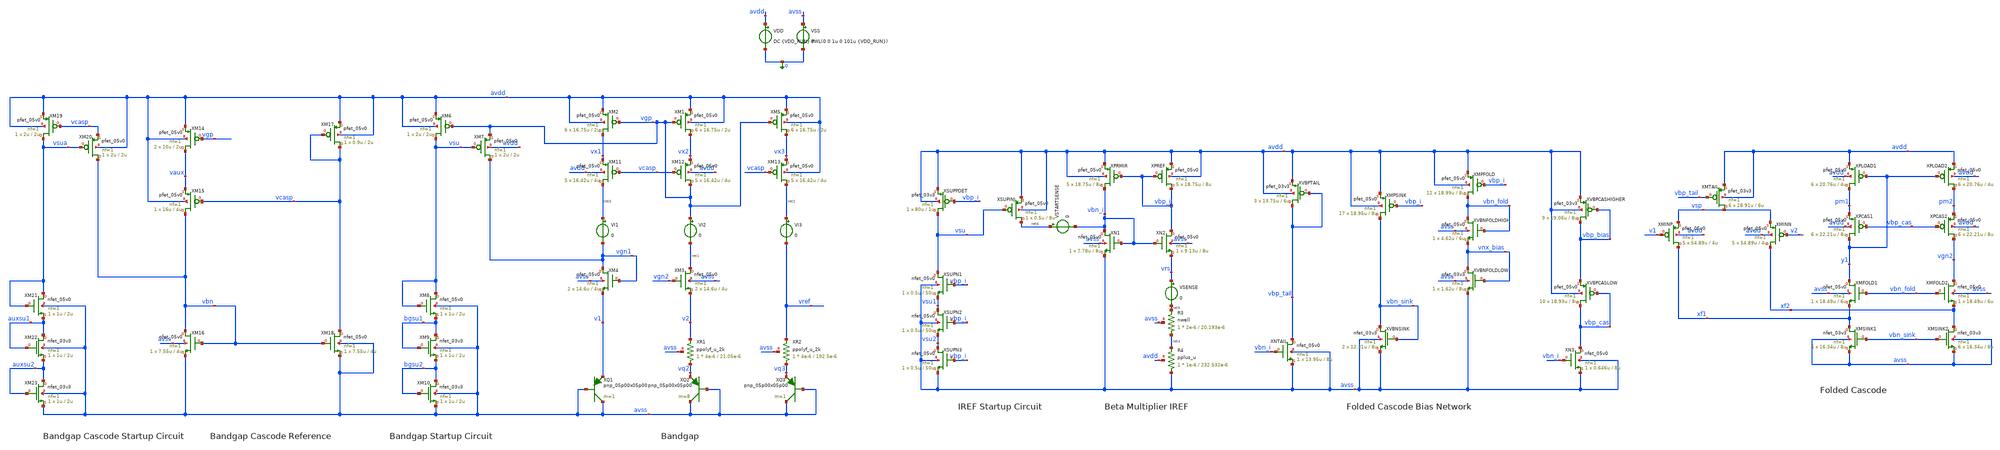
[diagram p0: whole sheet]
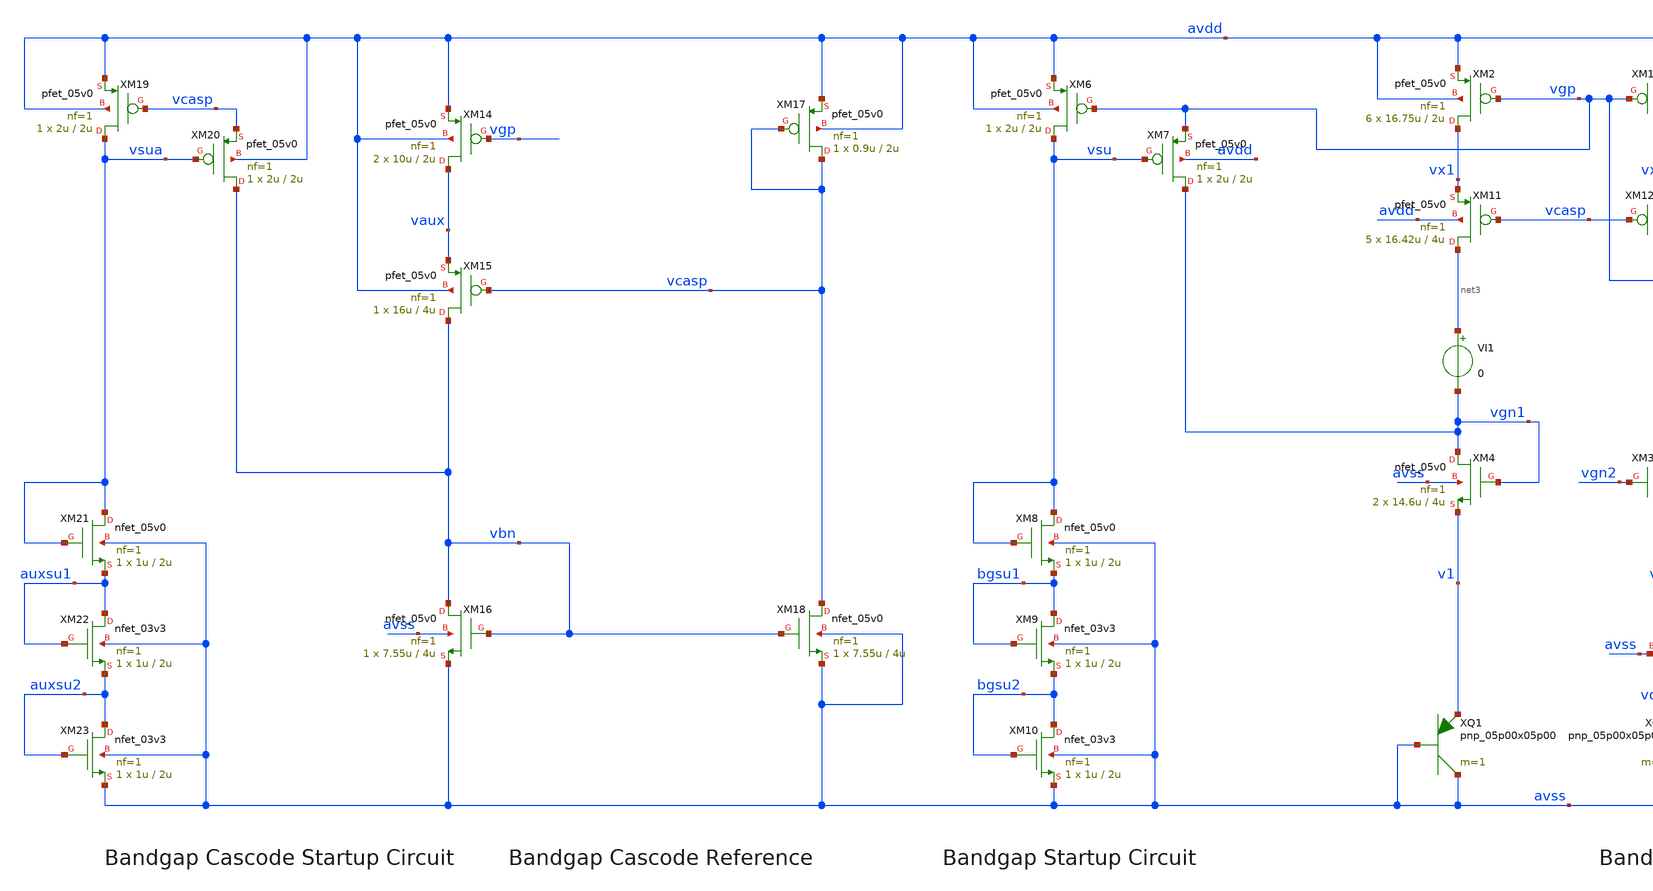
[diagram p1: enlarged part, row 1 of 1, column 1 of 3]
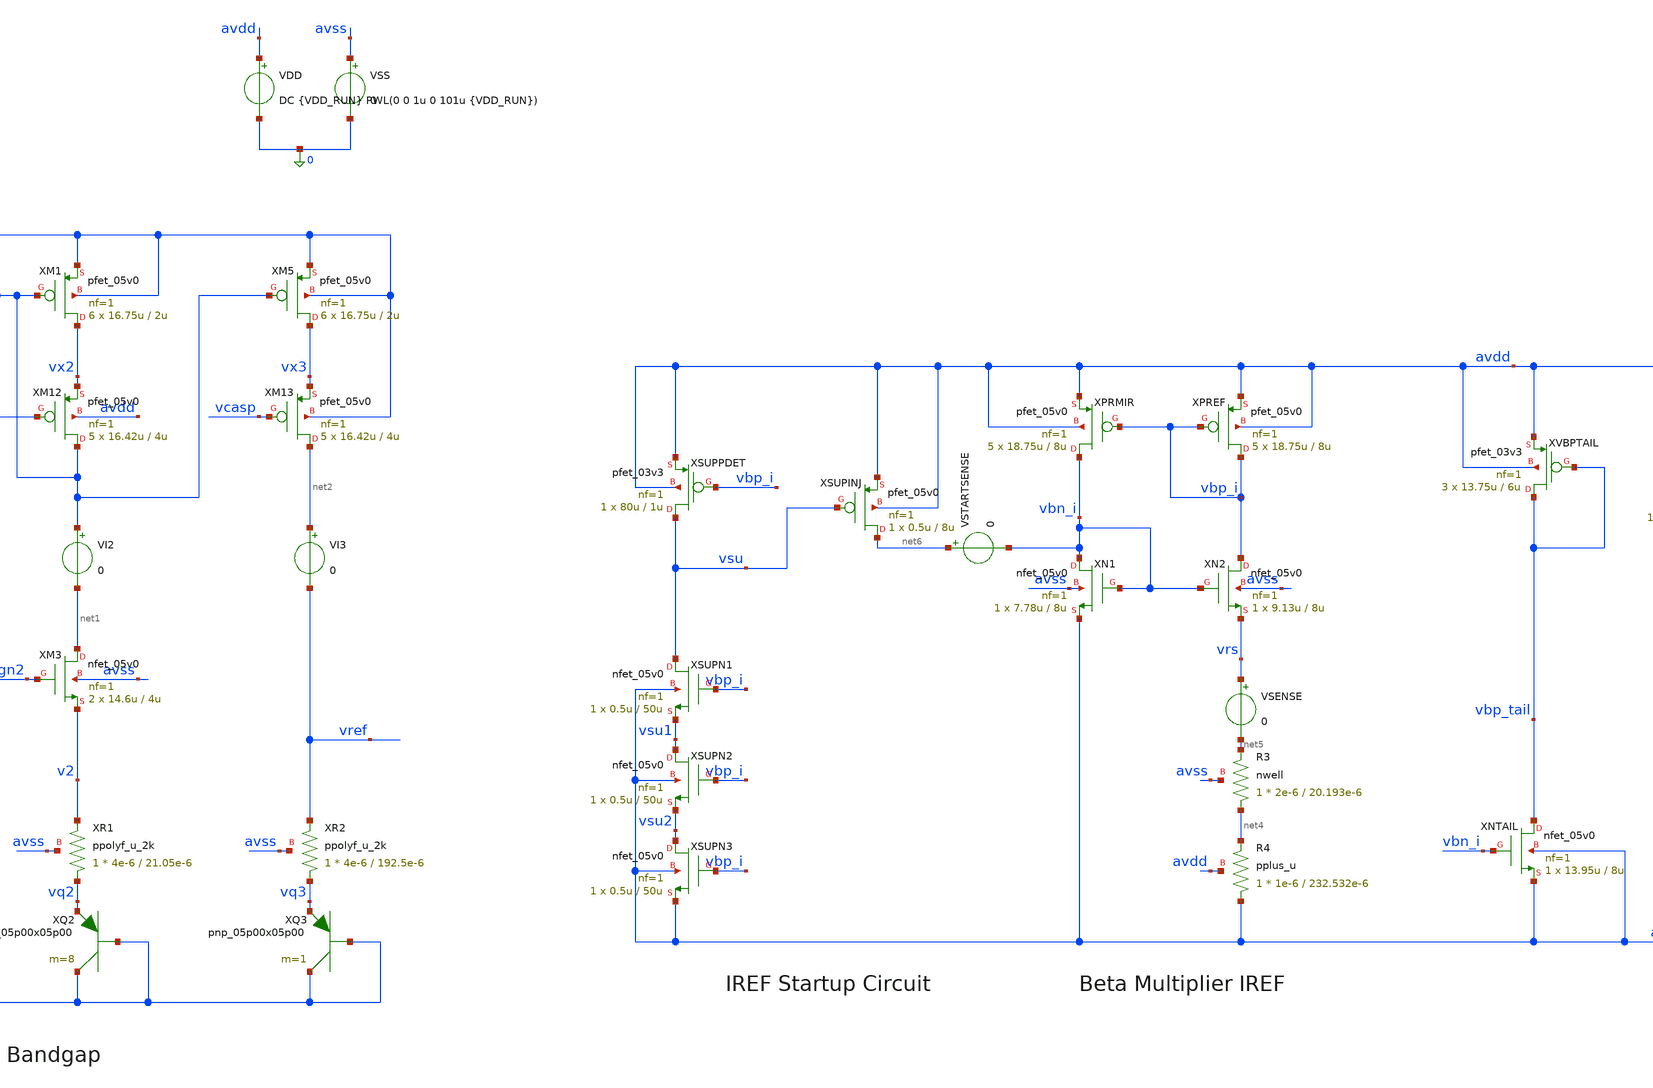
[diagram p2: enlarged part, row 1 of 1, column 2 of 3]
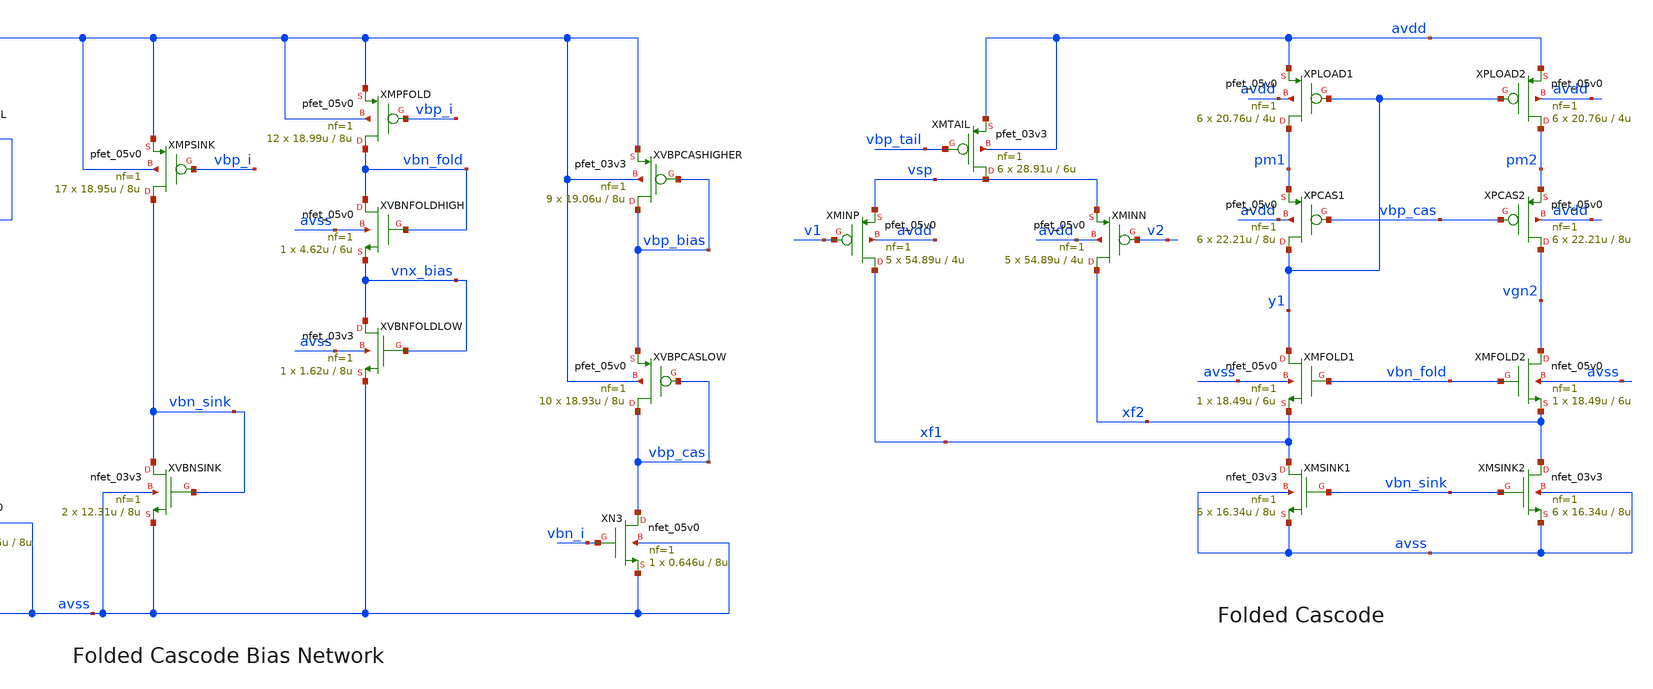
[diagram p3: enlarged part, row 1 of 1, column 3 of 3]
** sch_path: examples/gf180-bandgap/5vfullv2-original.sch
**.subckt 5vfullv2-original
XQ3 avss avss vq3 pnp_05p00x05p00 m=1
XQ2 avss avss vq2 pnp_05p00x05p00 m=8
XQ1 avss avss v1 pnp_05p00x05p00 m=1
XM9 bgsu1 bgsu1 bgsu2 avss nfet_03v3 L=2u W=1u nf=1 ad='int((nf+1)/2) * W/nf * 0.18u' as='int((nf+2)/2) * W/nf * 0.18u'
+ pd='2*int((nf+1)/2) * (W/nf + 0.18u)' ps='2*int((nf+2)/2) * (W/nf + 0.18u)' nrd='0.18u / W' nrs='0.18u / W'
+ sa=0 sb=0 sd=0 m=1
XM10 bgsu2 bgsu2 avss avss nfet_03v3 L=2u W=1u nf=1 ad='int((nf+1)/2) * W/nf * 0.18u' as='int((nf+2)/2) * W/nf * 0.18u'
+ pd='2*int((nf+1)/2) * (W/nf + 0.18u)' ps='2*int((nf+2)/2) * (W/nf + 0.18u)' nrd='0.18u / W' nrs='0.18u / W'
+ sa=0 sb=0 sd=0 m=1
XR1 vq2 v2 avss ppolyf_u_2k r_width=4e-6 r_length=21.05e-6 m=1
XR2 vq3 vref avss ppolyf_u_2k r_width=4e-6 r_length=192.5e-6 m=1
VI1 net3 vgn1 0
VI2 vgp net1 0
VI3 net2 vref 0
XM22 auxsu1 auxsu1 auxsu2 avss nfet_03v3 L=2u W=1u nf=1 ad='int((nf+1)/2) * W/nf * 0.18u' as='int((nf+2)/2) * W/nf * 0.18u'
+ pd='2*int((nf+1)/2) * (W/nf + 0.18u)' ps='2*int((nf+2)/2) * (W/nf + 0.18u)' nrd='0.18u / W' nrs='0.18u / W'
+ sa=0 sb=0 sd=0 m=1
XM23 auxsu2 auxsu2 avss avss nfet_03v3 L=2u W=1u nf=1 ad='int((nf+1)/2) * W/nf * 0.18u' as='int((nf+2)/2) * W/nf * 0.18u'
+ pd='2*int((nf+1)/2) * (W/nf + 0.18u)' ps='2*int((nf+2)/2) * (W/nf + 0.18u)' nrd='0.18u / W' nrs='0.18u / W'
+ sa=0 sb=0 sd=0 m=1
XMTAIL vsp vbp_tail avdd avdd pfet_03v3 L=6u W=28.91u nf=1 ad='int((nf+1)/2) * W/nf * 0.18u' as='int((nf+2)/2) * W/nf * 0.18u'
+ pd='2*int((nf+1)/2) * (W/nf + 0.18u)' ps='2*int((nf+2)/2) * (W/nf + 0.18u)' nrd='0.18u / W' nrs='0.18u / W'
+ sa=0 sb=0 sd=0 m=6
VDD avdd 0 DC {VDD_RUN} PWL(0 0 1u 0 101u {VDD_RUN})
VSS avss 0 0
XMSINK1 xf1 vbn_sink avss avss nfet_03v3 L=8u W=16.34u nf=1 ad='int((nf+1)/2) * W/nf * 0.18u' as='int((nf+2)/2) * W/nf * 0.18u'
+ pd='2*int((nf+1)/2) * (W/nf + 0.18u)' ps='2*int((nf+2)/2) * (W/nf + 0.18u)' nrd='0.18u / W' nrs='0.18u / W'
+ sa=0 sb=0 sd=0 m=6
XMSINK2 xf2 vbn_sink avss avss nfet_03v3 L=8u W=16.34u nf=1 ad='int((nf+1)/2) * W/nf * 0.18u' as='int((nf+2)/2) * W/nf * 0.18u'
+ pd='2*int((nf+1)/2) * (W/nf + 0.18u)' ps='2*int((nf+2)/2) * (W/nf + 0.18u)' nrd='0.18u / W' nrs='0.18u / W'
+ sa=0 sb=0 sd=0 m=6
XR3 net4 net5 avss nwell r_width=2e-6 r_length=20.193e-6 m=1
XR4 avss net4 avdd pplus_u r_width=1e-6 r_length=232.532e-6 m=1
VSENSE vrs net5 0
XSUPPDET vsu vbp_i avdd avdd pfet_03v3 L=1u W=80u nf=1 ad='int((nf+1)/2) * W/nf * 0.18u' as='int((nf+2)/2) * W/nf * 0.18u'
+ pd='2*int((nf+1)/2) * (W/nf + 0.18u)' ps='2*int((nf+2)/2) * (W/nf + 0.18u)' nrd='0.18u / W' nrs='0.18u / W'
+ sa=0 sb=0 sd=0 m=1
VSTARTSENSE net6 vbn_i 0
XPCAS2 vgn2 vbp_cas pm2 avdd pfet_05v0 L=8u W=22.21u nf=1 ad='int((nf+1)/2) * W/nf * 0.18u' as='int((nf+2)/2) * W/nf * 0.18u'
+ pd='2*int((nf+1)/2) * (W/nf + 0.18u)' ps='2*int((nf+2)/2) * (W/nf + 0.18u)' nrd='0.18u / W' nrs='0.18u / W'
+ sa=0 sb=0 sd=0 m=6
XPCAS1 y1 vbp_cas pm1 avdd pfet_05v0 L=8u W=22.21u nf=1 ad='int((nf+1)/2) * W/nf * 0.18u' as='int((nf+2)/2) * W/nf * 0.18u'
+ pd='2*int((nf+1)/2) * (W/nf + 0.18u)' ps='2*int((nf+2)/2) * (W/nf + 0.18u)' nrd='0.18u / W' nrs='0.18u / W'
+ sa=0 sb=0 sd=0 m=6
XMINN xf2 v2 vsp avdd pfet_05v0 L=4u W=54.89u nf=1 ad='int((nf+1)/2) * W/nf * 0.18u' as='int((nf+2)/2) * W/nf * 0.18u'
+ pd='2*int((nf+1)/2) * (W/nf + 0.18u)' ps='2*int((nf+2)/2) * (W/nf + 0.18u)' nrd='0.18u / W' nrs='0.18u / W'
+ sa=0 sb=0 sd=0 m=5
XMINP xf1 v1 vsp avdd pfet_05v0 L=4u W=54.89u nf=1 ad='int((nf+1)/2) * W/nf * 0.18u' as='int((nf+2)/2) * W/nf * 0.18u'
+ pd='2*int((nf+1)/2) * (W/nf + 0.18u)' ps='2*int((nf+2)/2) * (W/nf + 0.18u)' nrd='0.18u / W' nrs='0.18u / W'
+ sa=0 sb=0 sd=0 m=5
XMFOLD2 vgn2 vbn_fold xf2 avss nfet_05v0 L=6u W=18.49u nf=1 ad='int((nf+1)/2) * W/nf * 0.18u' as='int((nf+2)/2) * W/nf * 0.18u'
+ pd='2*int((nf+1)/2) * (W/nf + 0.18u)' ps='2*int((nf+2)/2) * (W/nf + 0.18u)' nrd='0.18u / W' nrs='0.18u / W'
+ sa=0 sb=0 sd=0 m=1
XMFOLD1 y1 vbn_fold xf1 avss nfet_05v0 L=6u W=18.49u nf=1 ad='int((nf+1)/2) * W/nf * 0.18u' as='int((nf+2)/2) * W/nf * 0.18u'
+ pd='2*int((nf+1)/2) * (W/nf + 0.18u)' ps='2*int((nf+2)/2) * (W/nf + 0.18u)' nrd='0.18u / W' nrs='0.18u / W'
+ sa=0 sb=0 sd=0 m=1
XN1 vbn_i vbn_i avss avss nfet_05v0 L=8u W=7.78u nf=1 ad='int((nf+1)/2) * W/nf * 0.18u' as='int((nf+2)/2) * W/nf * 0.18u'
+ pd='2*int((nf+1)/2) * (W/nf + 0.18u)' ps='2*int((nf+2)/2) * (W/nf + 0.18u)' nrd='0.18u / W' nrs='0.18u / W'
+ sa=0 sb=0 sd=0 m=1
XN2 vbp_i vbn_i vrs avss nfet_05v0 L=8u W=9.13u nf=1 ad='int((nf+1)/2) * W/nf * 0.18u' as='int((nf+2)/2) * W/nf * 0.18u'
+ pd='2*int((nf+1)/2) * (W/nf + 0.18u)' ps='2*int((nf+2)/2) * (W/nf + 0.18u)' nrd='0.18u / W' nrs='0.18u / W'
+ sa=0 sb=0 sd=0 m=1
XPREF vbp_i vbp_i avdd avdd pfet_05v0 L=8u W=18.75u nf=1 ad='int((nf+1)/2) * W/nf * 0.18u' as='int((nf+2)/2) * W/nf * 0.18u'
+ pd='2*int((nf+1)/2) * (W/nf + 0.18u)' ps='2*int((nf+2)/2) * (W/nf + 0.18u)' nrd='0.18u / W' nrs='0.18u / W'
+ sa=0 sb=0 sd=0 m=5
XPRMIR vbn_i vbp_i avdd avdd pfet_05v0 L=8u W=18.75u nf=1 ad='int((nf+1)/2) * W/nf * 0.18u' as='int((nf+2)/2) * W/nf * 0.18u'
+ pd='2*int((nf+1)/2) * (W/nf + 0.18u)' ps='2*int((nf+2)/2) * (W/nf + 0.18u)' nrd='0.18u / W' nrs='0.18u / W'
+ sa=0 sb=0 sd=0 m=5
XNTAIL vbp_tail vbn_i avss avss nfet_05v0 L=8u W=13.95u nf=1 ad='int((nf+1)/2) * W/nf * 0.18u' as='int((nf+2)/2) * W/nf * 0.18u'
+ pd='2*int((nf+1)/2) * (W/nf + 0.18u)' ps='2*int((nf+2)/2) * (W/nf + 0.18u)' nrd='0.18u / W' nrs='0.18u / W'
+ sa=0 sb=0 sd=0 m=1
XN3 vbp_cas vbn_i avss avss nfet_05v0 L=8u W=0.646u nf=1 ad='int((nf+1)/2) * W/nf * 0.18u' as='int((nf+2)/2) * W/nf * 0.18u'
+ pd='2*int((nf+1)/2) * (W/nf + 0.18u)' ps='2*int((nf+2)/2) * (W/nf + 0.18u)' nrd='0.18u / W' nrs='0.18u / W'
+ sa=0 sb=0 sd=0 m=1
XMPSINK vbn_sink vbp_i avdd avdd pfet_05v0 L=8u W=18.95u nf=1 ad='int((nf+1)/2) * W/nf * 0.18u' as='int((nf+2)/2) * W/nf * 0.18u'
+ pd='2*int((nf+1)/2) * (W/nf + 0.18u)' ps='2*int((nf+2)/2) * (W/nf + 0.18u)' nrd='0.18u / W' nrs='0.18u / W'
+ sa=0 sb=0 sd=0 m=17
XMPFOLD vbn_fold vbp_i avdd avdd pfet_05v0 L=8u W=18.99u nf=1 ad='int((nf+1)/2) * W/nf * 0.18u' as='int((nf+2)/2) * W/nf * 0.18u'
+ pd='2*int((nf+1)/2) * (W/nf + 0.18u)' ps='2*int((nf+2)/2) * (W/nf + 0.18u)' nrd='0.18u / W' nrs='0.18u / W'
+ sa=0 sb=0 sd=0 m=12
XVBNFOLDHIGH vbn_fold vbn_fold vnx_bias avss nfet_05v0 L=6u W=4.62u nf=1 ad='int((nf+1)/2) * W/nf * 0.18u'
+ as='int((nf+2)/2) * W/nf * 0.18u' pd='2*int((nf+1)/2) * (W/nf + 0.18u)' ps='2*int((nf+2)/2) * (W/nf + 0.18u)'
+ nrd='0.18u / W' nrs='0.18u / W' sa=0 sb=0 sd=0 m=1
XVBPCASLOW vbp_cas vbp_cas vbp_bias avdd pfet_05v0 L=8u W=18.93u nf=1 ad='int((nf+1)/2) * W/nf * 0.18u'
+ as='int((nf+2)/2) * W/nf * 0.18u' pd='2*int((nf+1)/2) * (W/nf + 0.18u)' ps='2*int((nf+2)/2) * (W/nf + 0.18u)'
+ nrd='0.18u / W' nrs='0.18u / W' sa=0 sb=0 sd=0 m=10
XVBNSINK vbn_sink vbn_sink avss avss nfet_03v3 L=8u W=12.31u nf=1 ad='int((nf+1)/2) * W/nf * 0.18u' as='int((nf+2)/2) * W/nf * 0.18u'
+ pd='2*int((nf+1)/2) * (W/nf + 0.18u)' ps='2*int((nf+2)/2) * (W/nf + 0.18u)' nrd='0.18u / W' nrs='0.18u / W'
+ sa=0 sb=0 sd=0 m=2
XVBPTAIL vbp_tail vbp_tail avdd avdd pfet_03v3 L=6u W=13.75u nf=1 ad='int((nf+1)/2) * W/nf * 0.18u' as='int((nf+2)/2) * W/nf * 0.18u'
+ pd='2*int((nf+1)/2) * (W/nf + 0.18u)' ps='2*int((nf+2)/2) * (W/nf + 0.18u)' nrd='0.18u / W' nrs='0.18u / W'
+ sa=0 sb=0 sd=0 m=3
XVBNFOLDLOW vnx_bias vnx_bias avss avss nfet_03v3 L=8u W=1.62u nf=1 ad='int((nf+1)/2) * W/nf * 0.18u'
+ as='int((nf+2)/2) * W/nf * 0.18u' pd='2*int((nf+1)/2) * (W/nf + 0.18u)' ps='2*int((nf+2)/2) * (W/nf + 0.18u)'
+ nrd='0.18u / W' nrs='0.18u / W' sa=0 sb=0 sd=0 m=1
XVBPCASHIGHER vbp_bias vbp_bias avdd avdd pfet_03v3 L=8u W=19.06u nf=1 ad='int((nf+1)/2) * W/nf * 0.18u'
+ as='int((nf+2)/2) * W/nf * 0.18u' pd='2*int((nf+1)/2) * (W/nf + 0.18u)' ps='2*int((nf+2)/2) * (W/nf + 0.18u)'
+ nrd='0.18u / W' nrs='0.18u / W' sa=0 sb=0 sd=0 m=9
XSUPN1 vsu vbp_i vsu1 avss nfet_05v0 L=50u W=0.5u nf=1 ad='int((nf+1)/2) * W/nf * 0.18u' as='int((nf+2)/2) * W/nf * 0.18u'
+ pd='2*int((nf+1)/2) * (W/nf + 0.18u)' ps='2*int((nf+2)/2) * (W/nf + 0.18u)' nrd='0.18u / W' nrs='0.18u / W'
+ sa=0 sb=0 sd=0 m=1
XSUPN2 vsu1 vbp_i vsu2 avss nfet_05v0 L=50u W=0.5u nf=1 ad='int((nf+1)/2) * W/nf * 0.18u' as='int((nf+2)/2) * W/nf * 0.18u'
+ pd='2*int((nf+1)/2) * (W/nf + 0.18u)' ps='2*int((nf+2)/2) * (W/nf + 0.18u)' nrd='0.18u / W' nrs='0.18u / W'
+ sa=0 sb=0 sd=0 m=1
XSUPN3 vsu2 vbp_i avss avss nfet_05v0 L=50u W=0.5u nf=1 ad='int((nf+1)/2) * W/nf * 0.18u' as='int((nf+2)/2) * W/nf * 0.18u'
+ pd='2*int((nf+1)/2) * (W/nf + 0.18u)' ps='2*int((nf+2)/2) * (W/nf + 0.18u)' nrd='0.18u / W' nrs='0.18u / W'
+ sa=0 sb=0 sd=0 m=1
XSUPINJ net6 vsu avdd avdd pfet_05v0 L=8u W=0.5u nf=1 ad='int((nf+1)/2) * W/nf * 0.18u' as='int((nf+2)/2) * W/nf * 0.18u'
+ pd='2*int((nf+1)/2) * (W/nf + 0.18u)' ps='2*int((nf+2)/2) * (W/nf + 0.18u)' nrd='0.18u / W' nrs='0.18u / W'
+ sa=0 sb=0 sd=0 m=1
XM11 net3 vcasp vx1 avdd pfet_05v0 L=4u W=16.42u nf=1 ad='int((nf+1)/2) * W/nf * 0.18u' as='int((nf+2)/2) * W/nf * 0.18u'
+ pd='2*int((nf+1)/2) * (W/nf + 0.18u)' ps='2*int((nf+2)/2) * (W/nf + 0.18u)' nrd='0.18u / W' nrs='0.18u / W'
+ sa=0 sb=0 sd=0 m=5
XM12 vgp vcasp vx2 avdd pfet_05v0 L=4u W=16.42u nf=1 ad='int((nf+1)/2) * W/nf * 0.18u' as='int((nf+2)/2) * W/nf * 0.18u'
+ pd='2*int((nf+1)/2) * (W/nf + 0.18u)' ps='2*int((nf+2)/2) * (W/nf + 0.18u)' nrd='0.18u / W' nrs='0.18u / W'
+ sa=0 sb=0 sd=0 m=5
XM13 net2 vcasp vx3 avdd pfet_05v0 L=4u W=16.42u nf=1 ad='int((nf+1)/2) * W/nf * 0.18u' as='int((nf+2)/2) * W/nf * 0.18u'
+ pd='2*int((nf+1)/2) * (W/nf + 0.18u)' ps='2*int((nf+2)/2) * (W/nf + 0.18u)' nrd='0.18u / W' nrs='0.18u / W'
+ sa=0 sb=0 sd=0 m=5
XM4 vgn1 vgn1 v1 avss nfet_05v0 L=4u W=14.6u nf=1 ad='int((nf+1)/2) * W/nf * 0.18u' as='int((nf+2)/2) * W/nf * 0.18u'
+ pd='2*int((nf+1)/2) * (W/nf + 0.18u)' ps='2*int((nf+2)/2) * (W/nf + 0.18u)' nrd='0.18u / W' nrs='0.18u / W'
+ sa=0 sb=0 sd=0 m=2
XM3 net1 vgn2 v2 avss nfet_05v0 L=4u W=14.6u nf=1 ad='int((nf+1)/2) * W/nf * 0.18u' as='int((nf+2)/2) * W/nf * 0.18u'
+ pd='2*int((nf+1)/2) * (W/nf + 0.18u)' ps='2*int((nf+2)/2) * (W/nf + 0.18u)' nrd='0.18u / W' nrs='0.18u / W'
+ sa=0 sb=0 sd=0 m=2
XM16 vbn vbn avss avss nfet_05v0 L=4u W=7.55u nf=1 ad='int((nf+1)/2) * W/nf * 0.18u' as='int((nf+2)/2) * W/nf * 0.18u'
+ pd='2*int((nf+1)/2) * (W/nf + 0.18u)' ps='2*int((nf+2)/2) * (W/nf + 0.18u)' nrd='0.18u / W' nrs='0.18u / W'
+ sa=0 sb=0 sd=0 m=1
XM18 vcasp vbn avss avss nfet_05v0 L=4u W=7.55u nf=1 ad='int((nf+1)/2) * W/nf * 0.18u' as='int((nf+2)/2) * W/nf * 0.18u'
+ pd='2*int((nf+1)/2) * (W/nf + 0.18u)' ps='2*int((nf+2)/2) * (W/nf + 0.18u)' nrd='0.18u / W' nrs='0.18u / W'
+ sa=0 sb=0 sd=0 m=1
XM15 vbn vcasp vaux avdd pfet_05v0 L=4u W=16u nf=1 ad='int((nf+1)/2) * W/nf * 0.18u' as='int((nf+2)/2) * W/nf * 0.18u'
+ pd='2*int((nf+1)/2) * (W/nf + 0.18u)' ps='2*int((nf+2)/2) * (W/nf + 0.18u)' nrd='0.18u / W' nrs='0.18u / W'
+ sa=0 sb=0 sd=0 m=1
XM17 vcasp vcasp avdd avdd pfet_05v0 L=2u W=0.9u nf=1 ad='int((nf+1)/2) * W/nf * 0.18u' as='int((nf+2)/2) * W/nf * 0.18u'
+ pd='2*int((nf+1)/2) * (W/nf + 0.18u)' ps='2*int((nf+2)/2) * (W/nf + 0.18u)' nrd='0.18u / W' nrs='0.18u / W'
+ sa=0 sb=0 sd=0 m=1
XM6 vsu vgp avdd avdd pfet_05v0 L=2u W=2u nf=1 ad='int((nf+1)/2) * W/nf * 0.18u' as='int((nf+2)/2) * W/nf * 0.18u'
+ pd='2*int((nf+1)/2) * (W/nf + 0.18u)' ps='2*int((nf+2)/2) * (W/nf + 0.18u)' nrd='0.18u / W' nrs='0.18u / W'
+ sa=0 sb=0 sd=0 m=1
XM7 vgn1 vsu vgp avdd pfet_05v0 L=2u W=2u nf=1 ad='int((nf+1)/2) * W/nf * 0.18u' as='int((nf+2)/2) * W/nf * 0.18u'
+ pd='2*int((nf+1)/2) * (W/nf + 0.18u)' ps='2*int((nf+2)/2) * (W/nf + 0.18u)' nrd='0.18u / W' nrs='0.18u / W'
+ sa=0 sb=0 sd=0 m=1
XM19 vsua vcasp avdd avdd pfet_05v0 L=2u W=2u nf=1 ad='int((nf+1)/2) * W/nf * 0.18u' as='int((nf+2)/2) * W/nf * 0.18u'
+ pd='2*int((nf+1)/2) * (W/nf + 0.18u)' ps='2*int((nf+2)/2) * (W/nf + 0.18u)' nrd='0.18u / W' nrs='0.18u / W'
+ sa=0 sb=0 sd=0 m=1
XM20 vbn vsua vcasp avdd pfet_05v0 L=2u W=2u nf=1 ad='int((nf+1)/2) * W/nf * 0.18u' as='int((nf+2)/2) * W/nf * 0.18u'
+ pd='2*int((nf+1)/2) * (W/nf + 0.18u)' ps='2*int((nf+2)/2) * (W/nf + 0.18u)' nrd='0.18u / W' nrs='0.18u / W'
+ sa=0 sb=0 sd=0 m=1
XM8 vsu vsu bgsu1 avss nfet_05v0 L=2u W=1u nf=1 ad='int((nf+1)/2) * W/nf * 0.18u' as='int((nf+2)/2) * W/nf * 0.18u'
+ pd='2*int((nf+1)/2) * (W/nf + 0.18u)' ps='2*int((nf+2)/2) * (W/nf + 0.18u)' nrd='0.18u / W' nrs='0.18u / W'
+ sa=0 sb=0 sd=0 m=1
XM21 vsua vsua auxsu1 avss nfet_05v0 L=2u W=1u nf=1 ad='int((nf+1)/2) * W/nf * 0.18u' as='int((nf+2)/2) * W/nf * 0.18u'
+ pd='2*int((nf+1)/2) * (W/nf + 0.18u)' ps='2*int((nf+2)/2) * (W/nf + 0.18u)' nrd='0.18u / W' nrs='0.18u / W'
+ sa=0 sb=0 sd=0 m=1
XPLOAD1 pm1 y1 avdd avdd pfet_05v0 L=4u W=20.76u nf=1 ad='int((nf+1)/2) * W/nf * 0.18u' as='int((nf+2)/2) * W/nf * 0.18u'
+ pd='2*int((nf+1)/2) * (W/nf + 0.18u)' ps='2*int((nf+2)/2) * (W/nf + 0.18u)' nrd='0.18u / W' nrs='0.18u / W'
+ sa=0 sb=0 sd=0 m=6
XPLOAD2 pm2 y1 avdd avdd pfet_05v0 L=4u W=20.76u nf=1 ad='int((nf+1)/2) * W/nf * 0.18u' as='int((nf+2)/2) * W/nf * 0.18u'
+ pd='2*int((nf+1)/2) * (W/nf + 0.18u)' ps='2*int((nf+2)/2) * (W/nf + 0.18u)' nrd='0.18u / W' nrs='0.18u / W'
+ sa=0 sb=0 sd=0 m=6
XM2 vx1 vgp avdd avdd pfet_05v0 L=2u W=16.75u nf=1 ad='int((nf+1)/2) * W/nf * 0.18u' as='int((nf+2)/2) * W/nf * 0.18u'
+ pd='2*int((nf+1)/2) * (W/nf + 0.18u)' ps='2*int((nf+2)/2) * (W/nf + 0.18u)' nrd='0.18u / W' nrs='0.18u / W'
+ sa=0 sb=0 sd=0 m=6
XM1 vx2 vgp avdd avdd pfet_05v0 L=2u W=16.75u nf=1 ad='int((nf+1)/2) * W/nf * 0.18u' as='int((nf+2)/2) * W/nf * 0.18u'
+ pd='2*int((nf+1)/2) * (W/nf + 0.18u)' ps='2*int((nf+2)/2) * (W/nf + 0.18u)' nrd='0.18u / W' nrs='0.18u / W'
+ sa=0 sb=0 sd=0 m=6
XM5 vx3 vgp avdd avdd pfet_05v0 L=2u W=16.75u nf=1 ad='int((nf+1)/2) * W/nf * 0.18u' as='int((nf+2)/2) * W/nf * 0.18u'
+ pd='2*int((nf+1)/2) * (W/nf + 0.18u)' ps='2*int((nf+2)/2) * (W/nf + 0.18u)' nrd='0.18u / W' nrs='0.18u / W'
+ sa=0 sb=0 sd=0 m=6
XM14 vaux vgp avdd avdd pfet_05v0 L=2u W=10u nf=1 ad='int((nf+1)/2) * W/nf * 0.18u' as='int((nf+2)/2) * W/nf * 0.18u'
+ pd='2*int((nf+1)/2) * (W/nf + 0.18u)' ps='2*int((nf+2)/2) * (W/nf + 0.18u)' nrd='0.18u / W' nrs='0.18u / W'
+ sa=0 sb=0 sd=0 m=2
**** begin user architecture code

* =====================================================================
* GF180 BANDGAP — FULL CHARACTERIZATION V5, 5-V-CAPABLE LOW-TC CORE
*
* Basis:
*   - latest cumulative handoff
*   - full2/full-characterization testbench structure
*   - current accepted rounded MOS geometry
*   - low-TC resistor point XR1=21.05 um, XR2=192.50 um
*
* REQUIRED FUNCTIONAL RANGE:
*   VDD = 3.0 to 5.0 V
*   T   = -40 to 125 C
*
* ROBUSTNESS ONLY:
*   VDD = 5.5 V
*
* WORKING SPEC TARGETS:
*   VREF            1.194 / 1.200 / 1.206 V
*   initial accuracy +/-0.5 %
*   IDD              20 / 30 / 50 uA  (project interpretation still open)
*   line regulation  0.01 / 0.05 / 0.1 % (endpoint interpretation used)
*   PSRR             60 / 70 / 80 dB   (frequency not yet specified)
*   noise            20 / 50 / 100 nV/sqrt(Hz) (frequency not yet specified)
*   TC               10 / 20 / 30 ppm/C
*   startup          50 / 100 / 200 us
*   IREF             180 / 220 / 260 nA
*
* IMPORTANT METHODOLOGY:
*   - clean DC/temp/line characterization uses fresh reset -> direct dc.
*   - no transient or op is allowed before authoritative clean DC sweeps.
*   - startup is characterized with a real supply ramp from 0 V.
*   - final startup leakage is SIGNED avg(i(VSTARTSENSE)).
*   - 5.5 V is reported separately and is not included in required-range
*     optimization/pass-fail.
*   - load tests are diagnostic only because no final load spec exists.
*   - output noise is intentionally in a separate validated-minimal deck.
*   - process corners are separate because .lib sections are parse-time.
*   - integrated loop gain is separate because the loop-break location must
*     be explicitly inserted/validated; do not infer PM from standalone OTA.
*
* OUTPUT DIRECTORY:
*   /foss/designs/chipalooza-bandgap/full_characterization_v5_5v
* =====================================================================

.include /foss/pdks/gf180mcuD/libs.tech/ngspice/design.ngspice
.lib /foss/pdks/gf180mcuD/libs.tech/ngspice/sm141064.ngspice typical
.lib /foss/pdks/gf180mcuD/libs.tech/ngspice/sm141064.ngspice bjt_typical
.lib /foss/pdks/gf180mcuD/libs.tech/ngspice/sm141064.ngspice res_typical

.options tnom=25

.param sw_stat_global=0
.param sw_stat_mismatch=0
.param fnoicor=0

* Current low-TC resistor target.  These parameters are documentary if the
* schematic uses fixed physical lengths.
.param XR1_L_UM=21.05
.param XR2_L_UM=192.50

.param VDD_RUN=5.0
.param P_ILOAD_DC=0
.param P_ILOAD_STEP=0
.param P_ZAC=0

* Testbench-only loads/injection.
ITBLOADDC   vref 0 DC {P_ILOAD_DC}
ITBLOADSTEP vref 0 PWL(0 0 2m 0 2001u {P_ILOAD_STEP} 2500u {P_ILOAD_STEP} 2501u 0)
ITBZ        vref 0 DC 0 AC {P_ZAC}

.control
set noaskquit
set numdgt=12
set wr_vecnames
set wr_singlescale

shell mkdir -p /foss/designs/chipalooza-bandgap/full_characterization_v5_5v

echo GF180_BANDGAP_FULL_CHARACTERIZATION_V5_5V >
+ /foss/designs/chipalooza-bandgap/full_characterization_v5_5v/README.txt
echo REQUIRED_VDD_3P0_TO_5P0_V >>
+ /foss/designs/chipalooza-bandgap/full_characterization_v5_5v/README.txt
echo VDD_5P5_IS_ROBUSTNESS_ONLY >>
+ /foss/designs/chipalooza-bandgap/full_characterization_v5_5v/README.txt
echo TEMP_RANGE_M40_TO_125_C >>
+ /foss/designs/chipalooza-bandgap/full_characterization_v5_5v/README.txt
echo XR1_21P05UM_XR2_192P50UM_LOW_TC_TARGET >>
+ /foss/designs/chipalooza-bandgap/full_characterization_v5_5v/README.txt
echo CLEAN_DC_IS_RESET_THEN_DIRECT_DC_NO_PRECEDING_TRAN_OR_OP >>
+ /foss/designs/chipalooza-bandgap/full_characterization_v5_5v/README.txt
echo STARTUP_FINAL_CURRENT_IS_SIGNED_AVG_I_VSTARTSENSE >>
+ /foss/designs/chipalooza-bandgap/full_characterization_v5_5v/README.txt
echo LOAD_TEST_IS_DIAGNOSTIC_NO_FINAL_LOAD_SPEC >>
+ /foss/designs/chipalooza-bandgap/full_characterization_v5_5v/README.txt
echo NOISE_AND_PROCESS_CORNERS_AND_MC_USE_COMPANION_DECKS >>
+ /foss/designs/chipalooza-bandgap/full_characterization_v5_5v/README.txt

* =====================================================================
* A. REQUIRED + ROBUSTNESS STARTUP MATRIX
*    6 VDD x 3 temperatures = 18 real power-up transients.
* =====================================================================
echo TEMP_C VDD_SET_V VDD_FINAL_V VREF_FINAL_V IREF_nA IDD_uA VERR_uV I1_uA I2_uA I3_uA G1 G3 VGP_V
+ VCASP_V VBN_V VGN1_V VGN2_V VSU_V VSUA_V START_PEAK_nA START_FINAL_SIGNED_nA TSETTLE_ABS_us
+ TSETTLE_AFTER_RAMP_us > /foss/designs/chipalooza-bandgap/full_characterization_v5_5v/startup_18pt.dat

foreach T -40 25 125
  foreach V 3.0 3.3 4.0 4.5 5.0 5.5
    alterparam VDD_RUN=$V
    alterparam P_ILOAD_DC=0
    alterparam P_ILOAD_STEP=0
    alterparam P_ZAC=0
    alterparam sw_stat_global=0
    alterparam sw_stat_mismatch=0
    alterparam fnoicor=0

    reset
    set temp=$T
    alter vdd dc=$V
    alter vdd acmag=0
    alter @vdd[pwl] = [ 0 0 1u 0 101u $V 3m $V ]
    alter itbloaddc dc=0
    alter @itbloadstep[pwl] = [ 0 0 3m 0 ]
    alter itbz acmag=0
    save all
    tran 50n 3m

    let IREF_RAW=abs(i(vsense))
    let IDD_RAW=-i(vdd)
    let VERR_RAW=v(v1)-v(v2)
    let I1_RAW=abs(i(vi1))
    let I2_RAW=abs(i(vi2))
    let I3_RAW=abs(i(vi3))
    let ISTART_RAW=i(vstartsense)
    let ISTART_ABS=abs(i(vstartsense))

    meas tran S_VDD avg v(avdd) from=2800u to=3000u
    meas tran S_VREF avg v(vref) from=2800u to=3000u
    meas tran S_IREF avg IREF_RAW from=2800u to=3000u
    meas tran S_IDD avg IDD_RAW from=2800u to=3000u
    meas tran S_VERR avg VERR_RAW from=2800u to=3000u
    meas tran S_I1 avg I1_RAW from=2800u to=3000u
    meas tran S_I2 avg I2_RAW from=2800u to=3000u
    meas tran S_I3 avg I3_RAW from=2800u to=3000u
    meas tran S_VGP avg v(vgp) from=2800u to=3000u
    meas tran S_VCASP avg v(vcasp) from=2800u to=3000u
    meas tran S_VBN avg v(vbn) from=2800u to=3000u
    meas tran S_VGN1 avg v(vgn1) from=2800u to=3000u
    meas tran S_VGN2 avg v(vgn2) from=2800u to=3000u
    meas tran S_VSU avg v(vsu) from=2800u to=3000u
    meas tran S_VSUA avg v(vsua) from=2800u to=3000u
    meas tran S_START_PK max ISTART_ABS from=0 to=500u
    meas tran S_START_FINAL avg ISTART_RAW from=2800u to=3000u

    let VREF_ERR=abs(v(vref)-S_VREF)
    meas tran S_SETTLE when VREF_ERR=1m fall=last

    let S_IREF_NA=S_IREF*1e9
    let S_IDD_UA=S_IDD*1e6
    let S_VERR_UV=S_VERR*1e6
    let S_I1_UA=S_I1*1e6
    let S_I2_UA=S_I2*1e6
    let S_I3_UA=S_I3*1e6
    let S_G1=S_I1/S_I2
    let S_G3=S_I3/S_I2
    let S_START_PK_NA=S_START_PK*1e9
    let S_START_FINAL_NA=S_START_FINAL*1e9
    let S_SETTLE_US=S_SETTLE*1e6
    let S_SETTLE_AFTER_US=(S_SETTLE-101u)*1e6

    echo $T $V $&S_VDD $&S_VREF $&S_IREF_NA $&S_IDD_UA $&S_VERR_UV $&S_I1_UA $&S_I2_UA $&S_I3_UA
+ $&S_G1 $&S_G3 $&S_VGP $&S_VCASP $&S_VBN $&S_VGN1 $&S_VGN2 $&S_VSU $&S_VSUA $&S_START_PK_NA
+ $&S_START_FINAL_NA $&S_SETTLE_US $&S_SETTLE_AFTER_US >>
+ /foss/designs/chipalooza-bandgap/full_characterization_v5_5v/startup_18pt.dat

    destroy all
  end
end

* =====================================================================
* B. AUTHORITATIVE CLEAN-DC LINE CURVES
*    Independent fresh reset at each temperature.
* =====================================================================

reset
set temp=-40
alterparam VDD_RUN=5.0
alterparam P_ILOAD_DC=0
alterparam P_ILOAD_STEP=0
alterparam P_ZAC=0
alterparam sw_stat_global=0
alterparam sw_stat_mismatch=0
alterparam fnoicor=0
alter vdd dc=5.0
alter vdd acmag=0
alter itbloaddc dc=0
alter itbz acmag=0
save all
dc vdd 3.0 5.6 0.05
let IREF_NA=abs(i(vsense))*1e9
let IDD_UA=-i(vdd)*1e6
let VERR_UV=(v(v1)-v(v2))*1e6
let I1_UA=abs(i(vi1))*1e6
let I2_UA=abs(i(vi2))*1e6
let I3_UA=abs(i(vi3))*1e6
let G1_VEC=I1_UA/I2_UA
let G3_VEC=I3_UA/I2_UA
wrdata /foss/designs/chipalooza-bandgap/full_characterization_v5_5v/clean_dc_m40C.dat v(vref)
+ IREF_NA IDD_UA VERR_UV G1_VEC G3_VEC
destroy all

reset
set temp=25
alterparam VDD_RUN=5.0
alterparam P_ILOAD_DC=0
alterparam P_ILOAD_STEP=0
alterparam P_ZAC=0
alterparam sw_stat_global=0
alterparam sw_stat_mismatch=0
alterparam fnoicor=0
alter vdd dc=5.0
alter vdd acmag=0
alter itbloaddc dc=0
alter itbz acmag=0
save all
dc vdd 3.0 5.6 0.05
let IREF_NA=abs(i(vsense))*1e9
let IDD_UA=-i(vdd)*1e6
let VERR_UV=(v(v1)-v(v2))*1e6
let I1_UA=abs(i(vi1))*1e6
let I2_UA=abs(i(vi2))*1e6
let I3_UA=abs(i(vi3))*1e6
let G1_VEC=I1_UA/I2_UA
let G3_VEC=I3_UA/I2_UA
wrdata /foss/designs/chipalooza-bandgap/full_characterization_v5_5v/clean_dc_25C.dat v(vref) IREF_NA
+ IDD_UA VERR_UV G1_VEC G3_VEC
destroy all

reset
set temp=125
alterparam VDD_RUN=5.0
alterparam P_ILOAD_DC=0
alterparam P_ILOAD_STEP=0
alterparam P_ZAC=0
alterparam sw_stat_global=0
alterparam sw_stat_mismatch=0
alterparam fnoicor=0
alter vdd dc=5.0
alter vdd acmag=0
alter itbloaddc dc=0
alter itbz acmag=0
save all
dc vdd 3.0 5.6 0.05
let IREF_NA=abs(i(vsense))*1e9
let IDD_UA=-i(vdd)*1e6
let VERR_UV=(v(v1)-v(v2))*1e6
let I1_UA=abs(i(vi1))*1e6
let I2_UA=abs(i(vi2))*1e6
let I3_UA=abs(i(vi3))*1e6
let G1_VEC=I1_UA/I2_UA
let G3_VEC=I3_UA/I2_UA
wrdata /foss/designs/chipalooza-bandgap/full_characterization_v5_5v/clean_dc_125C.dat v(vref)
+ IREF_NA IDD_UA VERR_UV G1_VEC G3_VEC
destroy all

* =====================================================================
* C. DENSE CLEAN-DC TEMPERATURE MATRIX
*    34 temperatures.  Each row comes from fresh reset -> direct DC.
* =====================================================================
echo TEMP_C VREF_3V0 VREF_3V3 VREF_4V0 VREF_4V5 VREF_5V0 VREF_5V5 IDD_uA_3V0 IDD_uA_3V3 IDD_uA_4V0
+ IDD_uA_4V5 IDD_uA_5V0 IDD_uA_5V5 IREF_nA_3V0 IREF_nA_3V3 IREF_nA_4V0 IREF_nA_4V5 IREF_nA_5V0 IREF_nA_5V5
+ VOS_uV_3V0 VOS_uV_3V3 VOS_uV_4V0 VOS_uV_4V5 VOS_uV_5V0 VOS_uV_5V5 >
+ /foss/designs/chipalooza-bandgap/full_characterization_v5_5v/dense_clean_dc_temperature.dat

foreach T -40 -35 -30 -25 -20 -15 -10 -5 0 5 10 15 20 25 30 35 40 45 50 55 60 65 70 75 80 85 90 95
+ 100 105 110 115 120 125
  alterparam VDD_RUN=5.0
  alterparam P_ILOAD_DC=0
  alterparam P_ILOAD_STEP=0
  alterparam P_ZAC=0
  alterparam sw_stat_global=0
  alterparam sw_stat_mismatch=0
  alterparam fnoicor=0

  reset
  set temp=$T
  alter vdd dc=5.0
  alter vdd acmag=0
  alter itbloaddc dc=0
  alter itbz acmag=0
  save all
  dc vdd 3.0 5.6 0.1

  let IDD_UA=-i(vdd)*1e6
  let IREF_NA=abs(i(vsense))*1e9
  let VOS_UV=(v(v2)-v(v1))*1e6

  meas dc VR30 find v(vref) at=3.0
  meas dc VR33 find v(vref) at=3.3
  meas dc VR40 find v(vref) at=4.0
  meas dc VR45 find v(vref) at=4.5
  meas dc VR50 find v(vref) at=5.0
  meas dc VR55 find v(vref) at=5.5

  meas dc ID30 find IDD_UA at=3.0
  meas dc ID33 find IDD_UA at=3.3
  meas dc ID40 find IDD_UA at=4.0
  meas dc ID45 find IDD_UA at=4.5
  meas dc ID50 find IDD_UA at=5.0
  meas dc ID55 find IDD_UA at=5.5

  meas dc IR30 find IREF_NA at=3.0
  meas dc IR33 find IREF_NA at=3.3
  meas dc IR40 find IREF_NA at=4.0
  meas dc IR45 find IREF_NA at=4.5
  meas dc IR50 find IREF_NA at=5.0
  meas dc IR55 find IREF_NA at=5.5

  meas dc VO30 find VOS_UV at=3.0
  meas dc VO33 find VOS_UV at=3.3
  meas dc VO40 find VOS_UV at=4.0
  meas dc VO45 find VOS_UV at=4.5
  meas dc VO50 find VOS_UV at=5.0
  meas dc VO55 find VOS_UV at=5.5

  echo $T $&VR30 $&VR33 $&VR40 $&VR45 $&VR50 $&VR55 $&ID30 $&ID33 $&ID40 $&ID45 $&ID50 $&ID55 $&IR30
+ $&IR33 $&IR40 $&IR45 $&IR50 $&IR55 $&VO30 $&VO33 $&VO40 $&VO45 $&VO50 $&VO55 >>
+ /foss/designs/chipalooza-bandgap/full_characterization_v5_5v/dense_clean_dc_temperature.dat

  destroy all
end

* =====================================================================
* D. STARTUP SUPPLY-RAMP SENSITIVITY
*    Required supply extremes, all key temperatures.
* =====================================================================
echo TEMP_C VDD_V TRAMP_S VREF_FINAL_V IREF_nA IDD_uA START_PEAK_nA START_FINAL_SIGNED_nA
+ TSETTLE_ABS_us TSETTLE_AFTER_RAMP_us >
+ /foss/designs/chipalooza-bandgap/full_characterization_v5_5v/startup_ramp_sensitivity.dat

foreach T -40 25 125
  foreach V 3.0 5.0
    foreach RAMP 1u 10u 100u 1m
      alterparam VDD_RUN=$V
      alterparam P_ILOAD_DC=0
      alterparam P_ILOAD_STEP=0
      alterparam P_ZAC=0
      alterparam sw_stat_global=0
      alterparam sw_stat_mismatch=0
      alterparam fnoicor=0

      reset
      set temp=$T
      let RAMP_END=1u+$RAMP
      alter vdd dc=$V
      alter vdd acmag=0
      alter @vdd[pwl] = [ 0 0 1u 0 $&RAMP_END $V 4m $V ]
      alter itbloaddc dc=0
      alter @itbloadstep[pwl] = [ 0 0 4m 0 ]
      alter itbz acmag=0
      save all
      tran 50n 4m

      let IREF_RAW=abs(i(vsense))
      let IDD_RAW=-i(vdd)
      let ISTART_RAW=i(vstartsense)
      let ISTART_ABS=abs(i(vstartsense))

      meas tran R_VREF avg v(vref) from=3800u to=4000u
      meas tran R_IREF avg IREF_RAW from=3800u to=4000u
      meas tran R_IDD avg IDD_RAW from=3800u to=4000u
      meas tran R_PK max ISTART_ABS from=0 to=1800u
      meas tran R_FINAL avg ISTART_RAW from=3800u to=4000u
      let VREF_ERR=abs(v(vref)-R_VREF)
      meas tran R_SETTLE when VREF_ERR=1m fall=last

      let R_IREF_NA=R_IREF*1e9
      let R_IDD_UA=R_IDD*1e6
      let R_PK_NA=R_PK*1e9
      let R_FINAL_NA=R_FINAL*1e9
      let R_SETTLE_US=R_SETTLE*1e6
      let R_AFTER_US=(R_SETTLE-RAMP_END)*1e6

      echo $T $V $RAMP $&R_VREF $&R_IREF_NA $&R_IDD_UA $&R_PK_NA $&R_FINAL_NA $&R_SETTLE_US
+ $&R_AFTER_US >> /foss/designs/chipalooza-bandgap/full_characterization_v5_5v/startup_ramp_sensitivity.dat

      destroy all
    end
  end
end

* =====================================================================
* E. LARGE-SIGNAL LINE TRANSIENT, 25 C
*    Required-range worst step: 3.0 -> 5.0 -> 3.0 V.
* =====================================================================
alterparam VDD_RUN=3.0
alterparam P_ILOAD_DC=0
alterparam P_ILOAD_STEP=0
alterparam P_ZAC=0
alterparam sw_stat_global=0
alterparam sw_stat_mismatch=0
alterparam fnoicor=0
reset
set temp=25
alter vdd dc=3.0
alter vdd acmag=0
alter @vdd[pwl] = [ 0 0 1u 0 101u 3.0 2m 3.0 2001u 5.0 2500u 5.0 2501u 3.0 3m 3.0 ]
alter itbloaddc dc=0
alter @itbloadstep[pwl] = [ 0 0 3m 0 ]
alter itbz acmag=0
save all
tran 20n 3m
let IDD_RAW=-i(vdd)
let VERR_RAW=v(v1)-v(v2)
wrdata
+ /foss/designs/chipalooza-bandgap/full_characterization_v5_5v/line_transient_3V_to_5V_to_3V_25C.dat time v(avdd) v(vref) VERR_RAW IDD_RAW
destroy all

* =====================================================================
* F. BROWNOUT / FULL POWER-CYCLE RESTART
* =====================================================================
echo TEMP_C VDD_V OFF_VDD_AVG_V VREF_AFTER_RESTART_V IREF_AFTER_RESTART_nA IDD_AFTER_RESTART_uA
+ START_RESTART_PEAK_nA START_FINAL_SIGNED_nA TSETTLE_RESTART_us >
+ /foss/designs/chipalooza-bandgap/full_characterization_v5_5v/brownout_restart.dat

foreach T -40 25 125
  foreach V 3.0 5.0 5.5
    alterparam VDD_RUN=$V
    alterparam P_ILOAD_DC=0
    alterparam P_ILOAD_STEP=0
    alterparam P_ZAC=0
    alterparam sw_stat_global=0
    alterparam sw_stat_mismatch=0
    alterparam fnoicor=0

    reset
    set temp=$T
    alter vdd dc=$V
    alter vdd acmag=0
    alter @vdd[pwl] = [ 0 0 1u 0 101u $V 4m $V 4001u 0 4500u 0 4501u $V 6m $V ]
    alter itbloaddc dc=0
    alter @itbloadstep[pwl] = [ 0 0 6m 0 ]
    alter itbz acmag=0
    save all
    tran 20n 6m

    let IREF_RAW=abs(i(vsense))
    let IDD_RAW=-i(vdd)
    let ISTART_RAW=i(vstartsense)
    let ISTART_ABS=abs(i(vstartsense))

    meas tran B_OFF avg v(avdd) from=4100u to=4400u
    meas tran B_VREF avg v(vref) from=5800u to=6000u
    meas tran B_IREF avg IREF_RAW from=5800u to=6000u
    meas tran B_IDD avg IDD_RAW from=5800u to=6000u
    meas tran B_PK max ISTART_ABS from=4500u to=5200u
    meas tran B_FINAL avg ISTART_RAW from=5800u to=6000u
    let VREF_ERR=abs(v(vref)-B_VREF)
    meas tran B_SETTLE when VREF_ERR=1m fall=last

    let B_IREF_NA=B_IREF*1e9
    let B_IDD_UA=B_IDD*1e6
    let B_PK_NA=B_PK*1e9
    let B_FINAL_NA=B_FINAL*1e9
    let B_SETTLE_RESTART_US=(B_SETTLE-4501u)*1e6

    echo $T $V $&B_OFF $&B_VREF $&B_IREF_NA $&B_IDD_UA $&B_PK_NA $&B_FINAL_NA $&B_SETTLE_RESTART_US
+ >> /foss/designs/chipalooza-bandgap/full_characterization_v5_5v/brownout_restart.dat

    destroy all
  end
end

* =====================================================================
* G. DC LOAD SENSITIVITY — DIAGNOSTIC ONLY, UNBUFFERED VREF
* =====================================================================
echo TEMP_C VDD_V ILOAD_A VREF_V IREF_nA IDD_uA VERR_uV >
+ /foss/designs/chipalooza-bandgap/full_characterization_v5_5v/load_regulation_diagnostic.dat

foreach T -40 25 125
  foreach V 3.0 5.0
    foreach LOAD 0 100n 250n 500n 1u
      alterparam VDD_RUN=$V
      alterparam P_ILOAD_DC=$LOAD
      alterparam P_ILOAD_STEP=0
      alterparam P_ZAC=0
      alterparam sw_stat_global=0
      alterparam sw_stat_mismatch=0
      alterparam fnoicor=0

      reset
      set temp=$T
      alter vdd dc=$V
      alter vdd acmag=0
      alter @vdd[pwl] = [ 0 0 1u 0 101u $V 3m $V ]
      alter itbloaddc dc=$LOAD
      alter @itbloadstep[pwl] = [ 0 0 3m 0 ]
      alter itbz acmag=0
      save all
      tran 50n 3m

      let IREF_RAW=abs(i(vsense))
      let IDD_RAW=-i(vdd)
      let VERR_RAW=v(v1)-v(v2)

      meas tran L_VREF avg v(vref) from=2800u to=3000u
      meas tran L_IREF avg IREF_RAW from=2800u to=3000u
      meas tran L_IDD avg IDD_RAW from=2800u to=3000u
      meas tran L_VERR avg VERR_RAW from=2800u to=3000u

      let L_IREF_NA=L_IREF*1e9
      let L_IDD_UA=L_IDD*1e6
      let L_VERR_UV=L_VERR*1e6

      echo $T $V $LOAD $&L_VREF $&L_IREF_NA $&L_IDD_UA $&L_VERR_UV >>
+ /foss/designs/chipalooza-bandgap/full_characterization_v5_5v/load_regulation_diagnostic.dat

      destroy all
    end
  end
end

* Nominal load-transient waveform: 0 -> 500 nA -> 0 at 5 V / 25 C.
alterparam VDD_RUN=5.0
alterparam P_ILOAD_DC=0
alterparam P_ILOAD_STEP=500n
alterparam P_ZAC=0
alterparam sw_stat_global=0
alterparam sw_stat_mismatch=0
alterparam fnoicor=0
reset
set temp=25
alter vdd dc=5.0
alter vdd acmag=0
alter @vdd[pwl] = [ 0 0 1u 0 101u 5.0 3m 5.0 ]
alter itbloaddc dc=0
alter @itbloadstep[pwl] = [ 0 0 2m 0 2001u 500n 2500u 500n 2501u 0 3m 0 ]
alter itbz acmag=0
save all
tran 20n 3m
wrdata /foss/designs/chipalooza-bandgap/full_characterization_v5_5v/load_transient_500nA_5V_25C.dat
+ time v(vref) v(v1) v(v2)
destroy all

* =====================================================================
* H. PSRR
*    AC=1 V on VDD. Report at representative decades.
*    The project target has no specified frequency, so this produces data
*    but does not silently claim a 60/70/80-dB pass at an undefined freq.
* =====================================================================
echo TEMP_C VDD_V PSRR_1Hz_dB PSRR_10Hz_dB PSRR_100Hz_dB PSRR_1kHz_dB PSRR_10kHz_dB PSRR_100kHz_dB
+ PSRR_1MHz_dB > /foss/designs/chipalooza-bandgap/full_characterization_v5_5v/psrr_keypoints.dat

foreach T -40 25 125
  foreach V 3.0 4.0 5.0
    alterparam VDD_RUN=$V
    alterparam P_ILOAD_DC=0
    alterparam P_ILOAD_STEP=0
    alterparam P_ZAC=0
    alterparam sw_stat_global=0
    alterparam sw_stat_mismatch=0
    alterparam fnoicor=0

    reset
    set temp=$T
    alter vdd dc=$V
    alter vdd acmag=1
    alter itbloaddc dc=0
    alter itbz acmag=0
    save all
    op
    ac dec 50 1 100Meg

    let VREF_AC_MAG=mag(v(vref))
    let PSRR_DB=-20*log10(VREF_AC_MAG+1e-30)

    meas ac P1 find PSRR_DB at=1
    meas ac P10 find PSRR_DB at=10
    meas ac P100 find PSRR_DB at=100
    meas ac P1K find PSRR_DB at=1k
    meas ac P10K find PSRR_DB at=10k
    meas ac P100K find PSRR_DB at=100k
    meas ac P1M find PSRR_DB at=1Meg

    echo $T $V $&P1 $&P10 $&P100 $&P1K $&P10K $&P100K $&P1M >>
+ /foss/designs/chipalooza-bandgap/full_characterization_v5_5v/psrr_keypoints.dat

    destroy all
  end
end

* Preserve a full nominal PSRR curve at 5 V / 25 C.
reset
set temp=25
alterparam VDD_RUN=5.0
alterparam P_ILOAD_DC=0
alterparam P_ILOAD_STEP=0
alterparam P_ZAC=0
alterparam sw_stat_global=0
alterparam sw_stat_mismatch=0
alterparam fnoicor=0
alter vdd dc=5.0
alter vdd acmag=1
alter itbloaddc dc=0
alter itbz acmag=0
save all
op
ac dec 50 1 100Meg
let VREF_AC_MAG=mag(v(vref))
let PSRR_DB=-20*log10(VREF_AC_MAG+1e-30)
wrdata /foss/designs/chipalooza-bandgap/full_characterization_v5_5v/psrr_5V_25C.dat PSRR_DB
+ VREF_AC_MAG
destroy all

* =====================================================================
* I. CLOSED-LOOP OUTPUT IMPEDANCE — DIAGNOSTIC
* =====================================================================
echo VDD_V ZOUT_1Hz_ohm ZOUT_10Hz_ohm ZOUT_100Hz_ohm ZOUT_1kHz_ohm ZOUT_10kHz_ohm ZOUT_100kHz_ohm
+ ZOUT_1MHz_ohm > /foss/designs/chipalooza-bandgap/full_characterization_v5_5v/output_impedance_keypoints.dat

foreach V 3.0 5.0
  alterparam VDD_RUN=$V
  alterparam P_ILOAD_DC=0
  alterparam P_ILOAD_STEP=0
  alterparam P_ZAC=1
  alterparam sw_stat_global=0
  alterparam sw_stat_mismatch=0
  alterparam fnoicor=0

  reset
  set temp=25
  alter vdd dc=$V
  alter vdd acmag=0
  alter itbloaddc dc=0
  alter itbz acmag=1
  save all
  op
  ac dec 50 1 10Meg

  let ZOUT_OHM=mag(v(vref))

  meas ac Z1 find ZOUT_OHM at=1
  meas ac Z10 find ZOUT_OHM at=10
  meas ac Z100 find ZOUT_OHM at=100
  meas ac Z1K find ZOUT_OHM at=1k
  meas ac Z10K find ZOUT_OHM at=10k
  meas ac Z100K find ZOUT_OHM at=100k
  meas ac Z1M find ZOUT_OHM at=1Meg

  echo $V $&Z1 $&Z10 $&Z100 $&Z1K $&Z10K $&Z100K $&Z1M >>
+ /foss/designs/chipalooza-bandgap/full_characterization_v5_5v/output_impedance_keypoints.dat

  destroy all
end

* Return to deterministic/no-test-load state.
alterparam VDD_RUN=5.0
alterparam P_ILOAD_DC=0
alterparam P_ILOAD_STEP=0
alterparam P_ZAC=0
alterparam sw_stat_global=0
alterparam sw_stat_mismatch=0
alterparam fnoicor=0

echo
echo =====================================================================
echo FULL_CHARACTERIZATION_V5_DETERMINISTIC_COMPLETE
echo Results:
echo /foss/designs/chipalooza-bandgap/full_characterization_v5_5v
echo Companion runs still required:
echo nominal_noise_minimal_v5
echo worst_flicker_noise_minimal_v5
echo process_corner_matrix
echo global_only_mismatch_only_combined_MC
echo integrated_loop_gain_after_valid_loop_break_is_inserted
echo =====================================================================
shell ls -lah /foss/designs/chipalooza-bandgap/full_characterization_v5_5v
rusage
.endc


**** end user architecture code
**.ends
.end
